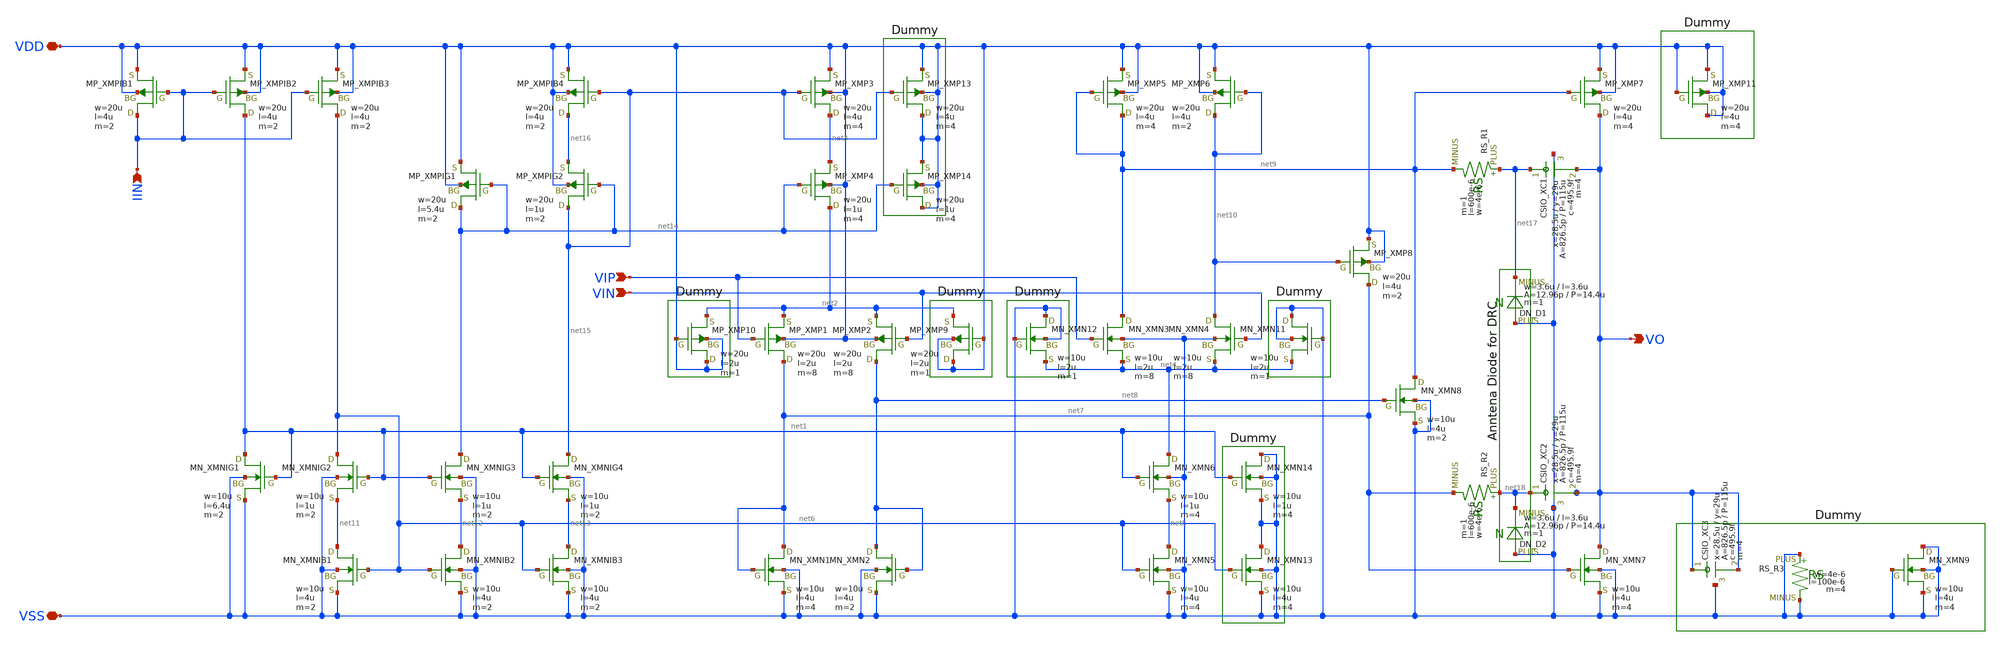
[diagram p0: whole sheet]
** sch_path: member_project/imager/YuMaehashi/design/amp_r2r.sch
**.subckt amp_r2r IIN VSS VDD VIN VIP VO
*.ipin IIN
*.iopin VSS
*.iopin VDD
*.ipin VIN
*.ipin VIP
*.opin VO
XXMNIG1 net1 net1 VSS VSS NMOS w=10u l=6.4u as=0 ad=0 ps=0 pd=0 nrd=0 nrs=0 m=2
XXMPIB1 IIN IIN VDD VDD PMOS w=20u l=4u as=0 ad=0 ps=0 pd=0 nrd=0 nrs=0 m=2
XXMP1 net7 VIP net2 VDD PMOS w=20u l=2u as=0 ad=0 ps=0 pd=0 nrd=0 nrs=0 m=8
XXMP2 net8 VIN net2 VDD PMOS w=20u l=2u as=0 ad=0 ps=0 pd=0 nrd=0 nrs=0 m=8
XXMP3 net3 net15 VDD VDD PMOS w=20u l=4u as=0 ad=0 ps=0 pd=0 nrd=0 nrs=0 m=4
XXMN3 net9 VIP net4 VSS NMOS w=10u l=2u as=0 ad=0 ps=0 pd=0 nrd=0 nrs=0 m=8
XXMN4 net10 VIN net4 VSS NMOS w=10u l=2u as=0 ad=0 ps=0 pd=0 nrd=0 nrs=0 m=8
XXMN5 net5 net6 VSS VSS NMOS w=10u l=4u as=0 ad=0 ps=0 pd=0 nrd=0 nrs=0 m=4
XXMN1 net7 net7 VSS VSS NMOS w=10u l=4u as=0 ad=0 ps=0 pd=0 nrd=0 nrs=0 m=4
XXMN2 net8 net8 VSS VSS NMOS w=10u l=4u as=0 ad=0 ps=0 pd=0 nrd=0 nrs=0 m=2
XXMP5 net9 net9 VDD VDD PMOS w=20u l=4u as=0 ad=0 ps=0 pd=0 nrd=0 nrs=0 m=4
XXMP6 net10 net10 VDD VDD PMOS w=20u l=4u as=0 ad=0 ps=0 pd=0 nrd=0 nrs=0 m=2
XXMP7 VO net9 VDD VDD PMOS w=20u l=4u as=0 ad=0 ps=0 pd=0 nrd=0 nrs=0 m=4
XXMN7 VO net7 VSS VSS NMOS w=10u l=4u as=0 ad=0 ps=0 pd=0 nrd=0 nrs=0 m=4
XXMN8 net9 net8 VSS VSS NMOS w=10u l=4u as=0 ad=0 ps=0 pd=0 nrd=0 nrs=0 m=2
XXMP8 net7 net10 VDD VDD PMOS w=20u l=4u as=0 ad=0 ps=0 pd=0 nrd=0 nrs=0 m=2
XXMPIB2 net1 IIN VDD VDD PMOS w=20u l=4u as=0 ad=0 ps=0 pd=0 nrd=0 nrs=0 m=2
XXMPIB3 net6 IIN VDD VDD PMOS w=20u l=4u as=0 ad=0 ps=0 pd=0 nrd=0 nrs=0 m=2
XXMNIG2 net6 net1 net11 VSS NMOS w=10u l=1u as=0 ad=0 ps=0 pd=0 nrd=0 nrs=0 m=2
XXMNIB1 net11 net6 VSS VSS NMOS w=10u l=4u as=0 ad=0 ps=0 pd=0 nrd=0 nrs=0 m=2
XXMNIB2 net12 net6 VSS VSS NMOS w=10u l=4u as=0 ad=0 ps=0 pd=0 nrd=0 nrs=0 m=2
XXMNIG3 net14 net1 net12 VSS NMOS w=10u l=1u as=0 ad=0 ps=0 pd=0 nrd=0 nrs=0 m=2
XXMNIB3 net13 net6 VSS VSS NMOS w=10u l=4u as=0 ad=0 ps=0 pd=0 nrd=0 nrs=0 m=2
XXMNIG4 net15 net1 net13 VSS NMOS w=10u l=1u as=0 ad=0 ps=0 pd=0 nrd=0 nrs=0 m=2
XXMPIG1 net14 net14 VDD VDD PMOS w=20u l=5.4u as=0 ad=0 ps=0 pd=0 nrd=0 nrs=0 m=2
XXMPIG2 net15 net14 net16 VDD PMOS w=20u l=1u as=0 ad=0 ps=0 pd=0 nrd=0 nrs=0 m=2
XXMPIB4 net16 net15 VDD VDD PMOS w=20u l=4u as=0 ad=0 ps=0 pd=0 nrd=0 nrs=0 m=2
XXMN6 net4 net1 net5 VSS NMOS w=10u l=1u as=0 ad=0 ps=0 pd=0 nrd=0 nrs=0 m=4
XXMP4 net2 net14 net3 VDD PMOS w=20u l=1u as=0 ad=0 ps=0 pd=0 nrd=0 nrs=0 m=4
XXC1 net17 VO VSS F_CSIO c=495.9f x=28.5u y=29u m=4
XXC2 net18 VO VSS F_CSIO c=495.9f x=28.5u y=29u m=4
XR1 net17 net9 F_RS w=4e-6 l=600e-6 R=1 tc1=0 tc2=0 m=1
XR2 net18 net7 F_RS w=4e-6 l=600e-6 R=1 tc1=0 tc2=0 m=1
XR3 VSS VSS F_RS w=4e-6 l=100e-6 R=1 tc1=0 tc2=0 m=4
XXMN9 VSS VSS VSS VSS NMOS w=10u l=4u as=0 ad=0 ps=0 pd=0 nrd=0 nrs=0 m=4
XXMN11 VSS VSS net4 VSS NMOS w=10u l=2u as=0 ad=0 ps=0 pd=0 nrd=0 nrs=0 m=1
XXMN12 VSS VSS net4 VSS NMOS w=10u l=2u as=0 ad=0 ps=0 pd=0 nrd=0 nrs=0 m=1
XXMP9 VDD VDD net2 VDD PMOS w=20u l=2u as=0 ad=0 ps=0 pd=0 nrd=0 nrs=0 m=1
XXMP10 VDD VDD net2 VDD PMOS w=20u l=2u as=0 ad=0 ps=0 pd=0 nrd=0 nrs=0 m=1
XXMP11 VDD VDD VDD VDD PMOS w=20u l=4u as=0 ad=0 ps=0 pd=0 nrd=0 nrs=0 m=4
DD1 VSS net17 DN m=1
DD2 VSS net18 DN m=1
XXMN13 VSS net6 VSS VSS NMOS w=10u l=4u as=0 ad=0 ps=0 pd=0 nrd=0 nrs=0 m=4
XXMN14 VSS net1 VSS VSS NMOS w=10u l=1u as=0 ad=0 ps=0 pd=0 nrd=0 nrs=0 m=4
XXMP13 VDD net15 VDD VDD PMOS w=20u l=4u as=0 ad=0 ps=0 pd=0 nrd=0 nrs=0 m=4
XXMP14 VDD net14 VDD VDD PMOS w=20u l=1u as=0 ad=0 ps=0 pd=0 nrd=0 nrs=0 m=4
XXC3 VO VO VSS F_CSIO c=495.9f x=28.5u y=29u m=4
**.ends
.end
